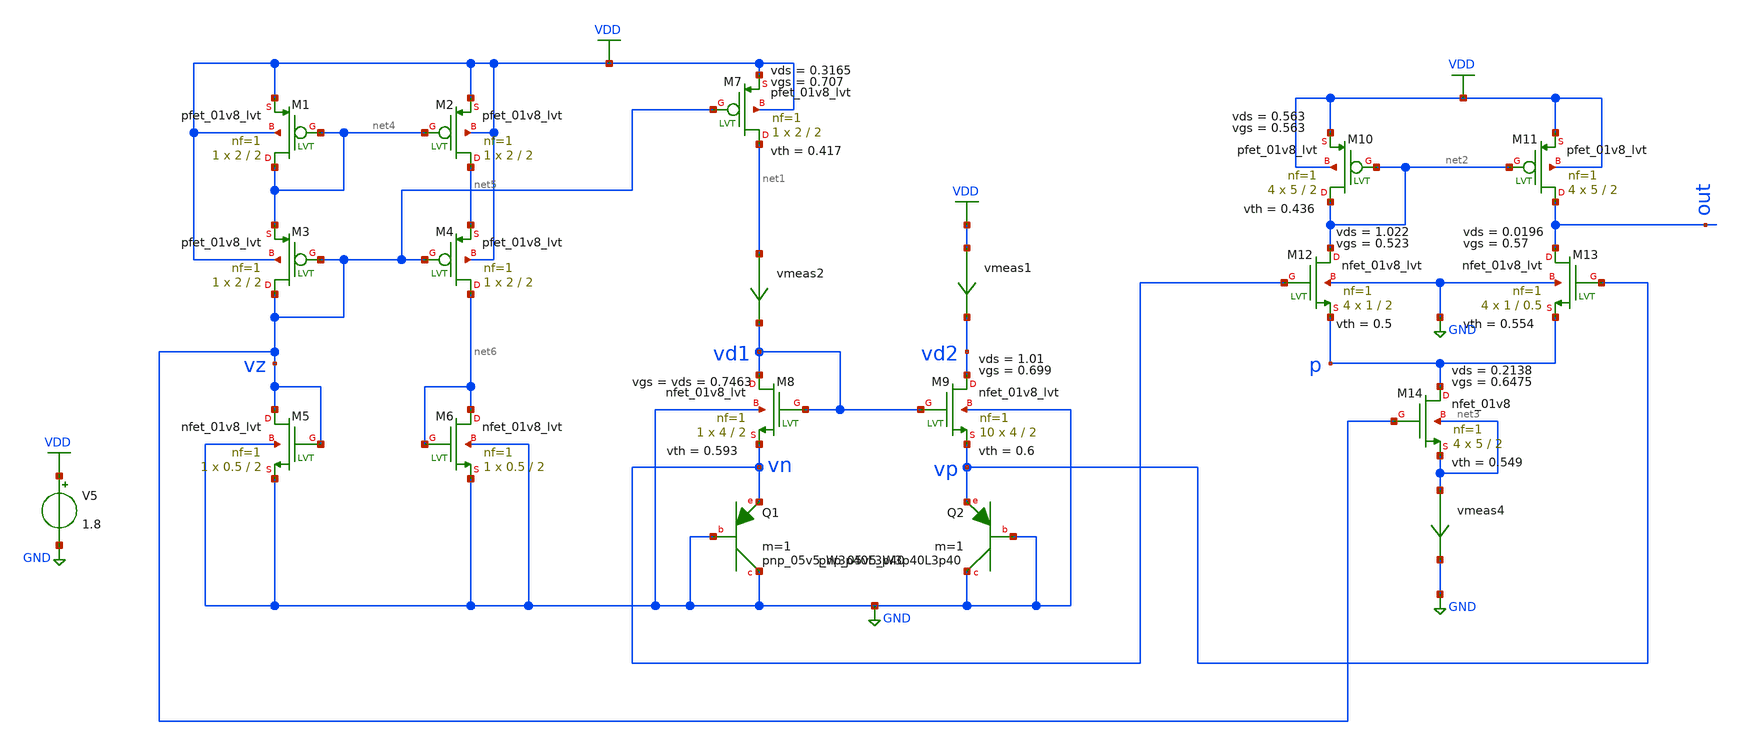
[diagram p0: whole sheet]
** sch_path: XSCHEM/Temp_Sensor_unbalanced_tb_op.sch
**.subckt Temp_Sensor_unbalanced_tb_op
V5 VDD GND 1.8
XM8 vd1 vd1 vn GND sky130_fd_pr__nfet_01v8_lvt L=2 W=4 nf=1 ad='int((nf+1)/2) * W/nf * 0.29' as='int((nf+2)/2) * W/nf * 0.29'
+ pd='2*int((nf+1)/2) * (W/nf + 0.29)' ps='2*int((nf+2)/2) * (W/nf + 0.29)' nrd='0.29 / W' nrs='0.29 / W'
+ sa=0 sb=0 sd=0 mult=1 m=1
XQ1 GND GND vn sky130_fd_pr__pnp_05v5_W3p40L3p40 m=1
XM9 vd2 vd1 vp GND sky130_fd_pr__nfet_01v8_lvt L=2 W=4 nf=1 ad='int((nf+1)/2) * W/nf * 0.29' as='int((nf+2)/2) * W/nf * 0.29'
+ pd='2*int((nf+1)/2) * (W/nf + 0.29)' ps='2*int((nf+2)/2) * (W/nf + 0.29)' nrd='0.29 / W' nrs='0.29 / W'
+ sa=0 sb=0 sd=0 mult=10 m=10
XQ2 GND GND vp sky130_fd_pr__pnp_05v5_W3p40L3p40 m=1
vmeas1 VDD vd2 0
.save i(vmeas1)
vmeas2 net1 vd1 0
.save i(vmeas2)
XM7 net1 vz VDD VDD sky130_fd_pr__pfet_01v8_lvt L=2 W=2 nf=1 ad='int((nf+1)/2) * W/nf * 0.29' as='int((nf+2)/2) * W/nf * 0.29'
+ pd='2*int((nf+1)/2) * (W/nf + 0.29)' ps='2*int((nf+2)/2) * (W/nf + 0.29)' nrd='0.29 / W' nrs='0.29 / W'
+ sa=0 sb=0 sd=0 mult=1 m=1
XM12 net2 vn p GND sky130_fd_pr__nfet_01v8_lvt L=2 W=1 nf=1 ad='int((nf+1)/2) * W/nf * 0.29' as='int((nf+2)/2) * W/nf * 0.29'
+ pd='2*int((nf+1)/2) * (W/nf + 0.29)' ps='2*int((nf+2)/2) * (W/nf + 0.29)' nrd='0.29 / W' nrs='0.29 / W'
+ sa=0 sb=0 sd=0 mult=4 m=4
XM13 out vp p GND sky130_fd_pr__nfet_01v8_lvt L=0.5 W=1 nf=1 ad='int((nf+1)/2) * W/nf * 0.29' as='int((nf+2)/2) * W/nf * 0.29'
+ pd='2*int((nf+1)/2) * (W/nf + 0.29)' ps='2*int((nf+2)/2) * (W/nf + 0.29)' nrd='0.29 / W' nrs='0.29 / W'
+ sa=0 sb=0 sd=0 mult=4 m=4
vmeas4 net3 GND 0
.save i(vmeas4)
XM14 p vz net3 net3 sky130_fd_pr__nfet_01v8 L=2 W=5 nf=1 ad='int((nf+1)/2) * W/nf * 0.29' as='int((nf+2)/2) * W/nf * 0.29'
+ pd='2*int((nf+1)/2) * (W/nf + 0.29)' ps='2*int((nf+2)/2) * (W/nf + 0.29)' nrd='0.29 / W' nrs='0.29 / W'
+ sa=0 sb=0 sd=0 mult=4 m=4
XM10 net2 net2 VDD VDD sky130_fd_pr__pfet_01v8_lvt L=2 W=5 nf=1 ad='int((nf+1)/2) * W/nf * 0.29' as='int((nf+2)/2) * W/nf * 0.29'
+ pd='2*int((nf+1)/2) * (W/nf + 0.29)' ps='2*int((nf+2)/2) * (W/nf + 0.29)' nrd='0.29 / W' nrs='0.29 / W'
+ sa=0 sb=0 sd=0 mult=4 m=4
XM11 out net2 VDD VDD sky130_fd_pr__pfet_01v8_lvt L=2 W=5 nf=1 ad='int((nf+1)/2) * W/nf * 0.29' as='int((nf+2)/2) * W/nf * 0.29'
+ pd='2*int((nf+1)/2) * (W/nf + 0.29)' ps='2*int((nf+2)/2) * (W/nf + 0.29)' nrd='0.29 / W' nrs='0.29 / W'
+ sa=0 sb=0 sd=0 mult=4 m=4
XM1 net4 net4 VDD VDD sky130_fd_pr__pfet_01v8_lvt L=2 W=2 nf=1 ad='int((nf+1)/2) * W/nf * 0.29' as='int((nf+2)/2) * W/nf * 0.29'
+ pd='2*int((nf+1)/2) * (W/nf + 0.29)' ps='2*int((nf+2)/2) * (W/nf + 0.29)' nrd='0.29 / W' nrs='0.29 / W'
+ sa=0 sb=0 sd=0 mult=1 m=1
XM5 vz vz GND GND sky130_fd_pr__nfet_01v8_lvt L=2 W=0.5 nf=1 ad='int((nf+1)/2) * W/nf * 0.29' as='int((nf+2)/2) * W/nf * 0.29'
+ pd='2*int((nf+1)/2) * (W/nf + 0.29)' ps='2*int((nf+2)/2) * (W/nf + 0.29)' nrd='0.29 / W' nrs='0.29 / W'
+ sa=0 sb=0 sd=0 mult=1 m=1
XM2 net5 net4 VDD VDD sky130_fd_pr__pfet_01v8_lvt L=2 W=2 nf=1 ad='int((nf+1)/2) * W/nf * 0.29' as='int((nf+2)/2) * W/nf * 0.29'
+ pd='2*int((nf+1)/2) * (W/nf + 0.29)' ps='2*int((nf+2)/2) * (W/nf + 0.29)' nrd='0.29 / W' nrs='0.29 / W'
+ sa=0 sb=0 sd=0 mult=1 m=1
XM4 net6 vz net5 VDD sky130_fd_pr__pfet_01v8_lvt L=2 W=2 nf=1 ad='int((nf+1)/2) * W/nf * 0.29' as='int((nf+2)/2) * W/nf * 0.29'
+ pd='2*int((nf+1)/2) * (W/nf + 0.29)' ps='2*int((nf+2)/2) * (W/nf + 0.29)' nrd='0.29 / W' nrs='0.29 / W'
+ sa=0 sb=0 sd=0 mult=1 m=1
XM3 vz vz net4 VDD sky130_fd_pr__pfet_01v8_lvt L=2 W=2 nf=1 ad='int((nf+1)/2) * W/nf * 0.29' as='int((nf+2)/2) * W/nf * 0.29'
+ pd='2*int((nf+1)/2) * (W/nf + 0.29)' ps='2*int((nf+2)/2) * (W/nf + 0.29)' nrd='0.29 / W' nrs='0.29 / W'
+ sa=0 sb=0 sd=0 mult=1 m=1
XM6 net6 net6 GND GND sky130_fd_pr__nfet_01v8_lvt L=2 W=0.5 nf=1 ad='int((nf+1)/2) * W/nf * 0.29' as='int((nf+2)/2) * W/nf * 0.29'
+ pd='2*int((nf+1)/2) * (W/nf + 0.29)' ps='2*int((nf+2)/2) * (W/nf + 0.29)' nrd='0.29 / W' nrs='0.29 / W'
+ sa=0 sb=0 sd=0 mult=1 m=1
**** begin user architecture code

.control
* Data to save
temp 50
save all  @M.XM1.msky130_fd_pr__pfet_01v8_lvt[id]  @M.XM1.msky130_fd_pr__pfet_01v8_lvt[vds]
+  @M.XM1.msky130_fd_pr__pfet_01v8_lvt[vgs]  @M.XM1.msky130_fd_pr__pfet_01v8_lvt[vth]  @M.XM2.msky130_fd_pr__pfet_01v8_lvt[id]
+  @M.XM2.msky130_fd_pr__pfet_01v8_lvt[vds]  @M.XM2.msky130_fd_pr__pfet_01v8_lvt[vgs]  @M.XM2.msky130_fd_pr__pfet_01v8_lvt[vth]
+  @M.XM3.msky130_fd_pr__pfet_01v8_lvt[id]  @M.XM3.msky130_fd_pr__pfet_01v8_lvt[vds]  @M.XM3.msky130_fd_pr__pfet_01v8_lvt[vgs]
+  @M.XM3.msky130_fd_pr__pfet_01v8_lvt[vth]  @M.XM4.msky130_fd_pr__pfet_01v8_lvt[id]  @M.XM4.msky130_fd_pr__pfet_01v8_lvt[vds]
+  @M.XM4.msky130_fd_pr__pfet_01v8_lvt[vgs]  @M.XM4.msky130_fd_pr__pfet_01v8_lvt[vth]  @M.XM5.msky130_fd_pr__nfet_01v8_lvt[id]
+  @M.XM5.msky130_fd_pr__nfet_01v8_lvt[vds]  @M.XM5.msky130_fd_pr__nfet_01v8_lvt[vgs]  @M.XM5.msky130_fd_pr__nfet_01v8_lvt[vth]
+  @M.XM6.msky130_fd_pr__nfet_01v8_lvt[id]  @M.XM6.msky130_fd_pr__nfet_01v8_lvt[vds]  @M.XM6.msky130_fd_pr__nfet_01v8_lvt[vgs]
+  @M.XM6.msky130_fd_pr__nfet_01v8_lvt[vth]  @M.XM7.msky130_fd_pr__pfet_01v8_lvt[id]  @M.XM7.msky130_fd_pr__pfet_01v8_lvt[vds]
+  @M.XM7.msky130_fd_pr__pfet_01v8_lvt[vgs]  @M.XM7.msky130_fd_pr__pfet_01v8_lvt[vth]  @M.XM8.msky130_fd_pr__nfet_01v8_lvt[id]
+  @M.XM8.msky130_fd_pr__nfet_01v8_lvt[vds]  @M.XM8.msky130_fd_pr__nfet_01v8_lvt[vgs]  @M.XM8.msky130_fd_pr__nfet_01v8_lvt[vth]
+  @M.XM9.msky130_fd_pr__nfet_01v8_lvt[id]  @M.XM9.msky130_fd_pr__nfet_01v8_lvt[vds]  @M.XM9.msky130_fd_pr__nfet_01v8_lvt[vgs]
+  @M.XM9.msky130_fd_pr__nfet_01v8_lvt[vth]  @M.XM10.msky130_fd_pr__pfet_01v8_lvt[id]  @M.XM10.msky130_fd_pr__pfet_01v8_lvt[vds]
+  @M.XM10.msky130_fd_pr__pfet_01v8_lvt[vgs]  @M.XM10.msky130_fd_pr__pfet_01v8_lvt[vth]  @M.XM11.msky130_fd_pr__pfet_01v8_lvt[id]
+  @M.XM11.msky130_fd_pr__pfet_01v8_lvt[vds]  @M.XM11.msky130_fd_pr__pfet_01v8_lvt[vgs]  @M.XM11.msky130_fd_pr__pfet_01v8_lvt[vth]
+  @M.XM12.msky130_fd_pr__nfet_01v8_lvt[id]  @M.XM12.msky130_fd_pr__nfet_01v8_lvt[vds]  @M.XM12.msky130_fd_pr__nfet_01v8_lvt[vgs]
+  @M.XM12.msky130_fd_pr__nfet_01v8_lvt[vth]  @M.XM13.msky130_fd_pr__nfet_01v8_lvt[id]  @M.XM13.msky130_fd_pr__nfet_01v8_lvt[vds]
+  @M.XM13.msky130_fd_pr__nfet_01v8_lvt[vgs]  @M.XM13.msky130_fd_pr__nfet_01v8_lvt[vth]  @M.XM14.msky130_fd_pr__nfet_01v8[id]
+  @M.XM14.msky130_fd_pr__nfet_01v8[vds]  @M.XM14.msky130_fd_pr__nfet_01v8[vgs]  @M.XM14.msky130_fd_pr__nfet_01v8[vth]

op

print @M.XM1.msky130_fd_pr__pfet_01v8_lvt[id]
print @M.XM1.msky130_fd_pr__pfet_01v8_lvt[vds]
print @M.XM1.msky130_fd_pr__pfet_01v8_lvt[vgs]
print @M.XM1.msky130_fd_pr__pfet_01v8_lvt[vth]
print @M.XM2.msky130_fd_pr__pfet_01v8_lvt[id]
print @M.XM2.msky130_fd_pr__pfet_01v8_lvt[vds]
print @M.XM2.msky130_fd_pr__pfet_01v8_lvt[vgs]
print @M.XM2.msky130_fd_pr__pfet_01v8_lvt[vth]
print @M.XM3.msky130_fd_pr__pfet_01v8_lvt[id]
print @M.XM3.msky130_fd_pr__pfet_01v8_lvt[vds]
print @M.XM3.msky130_fd_pr__pfet_01v8_lvt[vgs]
print @M.XM3.msky130_fd_pr__pfet_01v8_lvt[vth]
print @M.XM4.msky130_fd_pr__pfet_01v8_lvt[id]
print @M.XM4.msky130_fd_pr__pfet_01v8_lvt[vds]
print @M.XM4.msky130_fd_pr__pfet_01v8_lvt[vgs]
print @M.XM4.msky130_fd_pr__pfet_01v8_lvt[vth]
print @M.XM5.msky130_fd_pr__nfet_01v8_lvt[id]
print @M.XM5.msky130_fd_pr__nfet_01v8_lvt[vds]
print @M.XM5.msky130_fd_pr__nfet_01v8_lvt[vgs]
print @M.XM5.msky130_fd_pr__nfet_01v8_lvt[vth]
print @M.XM6.msky130_fd_pr__nfet_01v8_lvt[id]
print @M.XM6.msky130_fd_pr__nfet_01v8_lvt[vds]
print @M.XM6.msky130_fd_pr__nfet_01v8_lvt[vgs]
print @M.XM6.msky130_fd_pr__nfet_01v8_lvt[vth]
print @M.XM7.msky130_fd_pr__pfet_01v8_lvt[id]
print @M.XM7.msky130_fd_pr__pfet_01v8_lvt[vds]
print @M.XM7.msky130_fd_pr__pfet_01v8_lvt[vgs]
print @M.XM7.msky130_fd_pr__pfet_01v8_lvt[vth]
print @M.XM8.msky130_fd_pr__nfet_01v8_lvt[id]
print @M.XM8.msky130_fd_pr__nfet_01v8_lvt[vds]
print @M.XM8.msky130_fd_pr__nfet_01v8_lvt[vgs]
print @M.XM8.msky130_fd_pr__nfet_01v8_lvt[vth]
print @M.XM9.msky130_fd_pr__nfet_01v8_lvt[id]
print @M.XM9.msky130_fd_pr__nfet_01v8_lvt[vds]
print @M.XM9.msky130_fd_pr__nfet_01v8_lvt[vgs]
print @M.XM9.msky130_fd_pr__nfet_01v8_lvt[vth]
print @M.XM10.msky130_fd_pr__pfet_01v8_lvt[id]
print @M.XM10.msky130_fd_pr__pfet_01v8_lvt[vds]
print @M.XM10.msky130_fd_pr__pfet_01v8_lvt[vgs]
print @M.XM10.msky130_fd_pr__pfet_01v8_lvt[vth]
print @M.XM11.msky130_fd_pr__pfet_01v8_lvt[id]
print @M.XM11.msky130_fd_pr__pfet_01v8_lvt[vds]
print @M.XM11.msky130_fd_pr__pfet_01v8_lvt[vgs]
print @M.XM11.msky130_fd_pr__pfet_01v8_lvt[vth]
print @M.XM12.msky130_fd_pr__nfet_01v8_lvt[id]
print @M.XM12.msky130_fd_pr__nfet_01v8_lvt[vds]
print @M.XM12.msky130_fd_pr__nfet_01v8_lvt[vgs]
print @M.XM12.msky130_fd_pr__nfet_01v8_lvt[vth]
print @M.XM13.msky130_fd_pr__nfet_01v8_lvt[id]
print @M.XM13.msky130_fd_pr__nfet_01v8_lvt[vds]
print @M.XM13.msky130_fd_pr__nfet_01v8_lvt[vgs]
print @M.XM13.msky130_fd_pr__nfet_01v8_lvt[vth]
print @M.XM14.msky130_fd_pr__nfet_01v8[id]
print @M.XM14.msky130_fd_pr__nfet_01v8[vds]
print @M.XM14.msky130_fd_pr__nfet_01v8[vgs]
print @M.XM14.msky130_fd_pr__nfet_01v8[vth]

.endc



** opencircuitdesign pdks install
.lib $::SKYWATER_MODELS/sky130.lib.spice tt


**** end user architecture code
**.ends
.GLOBAL VDD
.GLOBAL GND
.end
